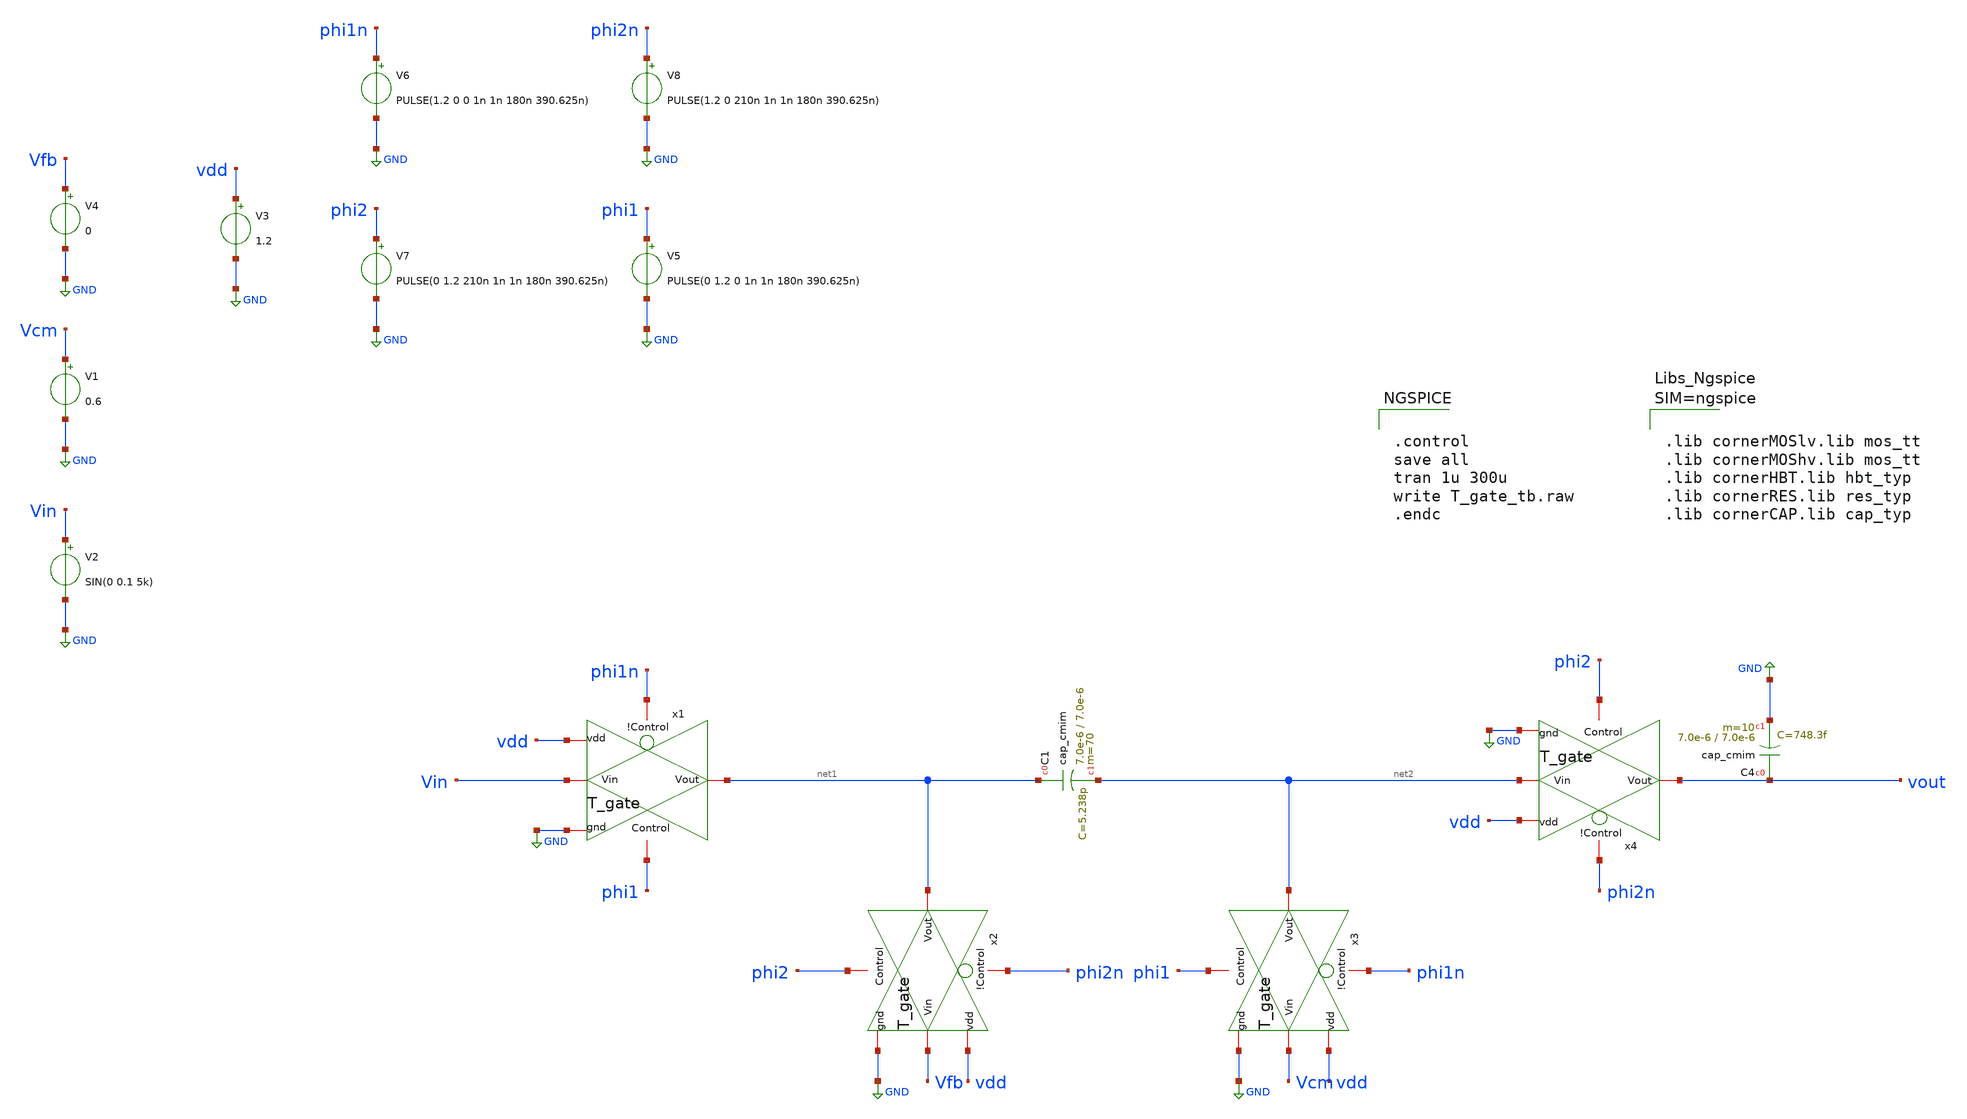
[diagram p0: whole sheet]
** sch_path: xschem/SC_integrator_tb.sch
**.subckt SC_integrator_tb
x1 phi1n Vin net1 GND phi1 vdd T_gate
x2 phi2n Vfb net1 GND phi2 vdd T_gate
x3 phi1n Vcm net2 GND phi1 vdd T_gate
XC1 net1 net2 cap_cmim w=7.0e-6 l=7.0e-6 m=70 mm_ok=1
x4 phi2n net2 vout GND phi2 vdd T_gate
V1 Vcm GND 0.6
V2 Vin GND SIN(0 0.1 5k)
V3 vdd GND 1.2
V4 Vfb GND 0
V5 phi1 GND PULSE(0 1.2 0 1n 1n 180n 390.625n)
V6 phi1n GND PULSE(1.2 0 0 1n 1n 180n 390.625n)
V7 phi2 GND PULSE(0 1.2 210n 1n 1n 180n 390.625n)
V8 phi2n GND PULSE(1.2 0 210n 1n 1n 180n 390.625n)
XC4 vout GND cap_cmim w=7.0e-6 l=7.0e-6 m=10 mm_ok=1
**** begin user architecture code


.control
save all
tran 1u 300u
write T_gate_tb.raw
.endc





.lib cornerMOSlv.lib mos_tt
.lib cornerMOShv.lib mos_tt
.lib cornerHBT.lib hbt_typ
.lib cornerRES.lib res_typ
.lib cornerCAP.lib cap_typ



**** end user architecture code
**.ends

* expanding   symbol:  T_gate.sym # of pins=6
** sym_path: T_gate.sym
** sch_path: T_gate.sch
.subckt T_gate !Control Vin Vout gnd Control vdd
*.iopin Vout
*.iopin Vin
*.iopin !Control
*.iopin Control
*.iopin gnd
*.iopin vdd
XM1 Vin Control Vout gnd sg13_lv_nmos w=1u l=0.13u ng=1 m=1 mm_ok=1
XM2 Vout !Control Vin vdd sg13_lv_pmos w=3u l=0.13u ng=1 m=1 mm_ok=1
.ends

.GLOBAL GND
.end
